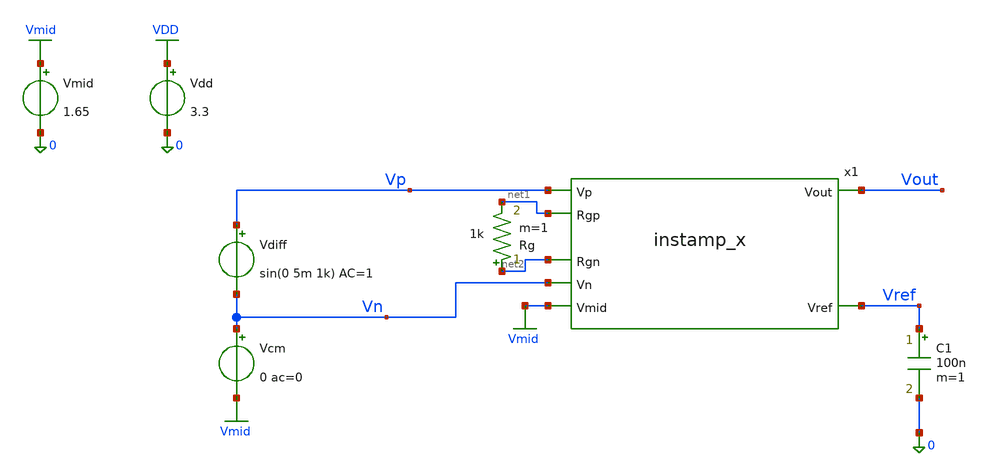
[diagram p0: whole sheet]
** sch_path: xschem/instamp_x_tb.sch
* Copyright 2021 Stefan Frederik Schippers
* Licensed under the Apache License, Version 2.0 (the "License");
* you may not use this file except in compliance with the License.
* You may obtain a copy of the License at
* https://www.apache.org/licenses/LICENSE-2.0
* Unless required by applicable law or agreed to in writing, software
* distributed under the License is distributed on an "AS IS" BASIS,
* WITHOUT WARRANTIES OR CONDITIONS OF ANY KIND, either express or implied.
* See the License for the specific language governing permissions and
* limitations under the License.
**.subckt instamp_x_tb
Vdd VDD 0 3.3
C1 Vref 0 100n m=1
Vdiff Vp Vn sin(0 5m 1k) AC=1
Vmid Vmid 0 1.65
x1 Vp Vmid net1 Vout Vref Vn net2 instamp_x
Rg net2 net1 1k m=1
Vcm Vn Vmid 0 ac=0
**** begin user architecture code

** opencircuitdesign pdks install
.lib $::SKYWATER_MODELS/sky130.lib.spice tt



.option wnflag=1
.option savecurrents
.save all
.control
op
write instamp_x_tb.raw
set appendwrite
set gnuplot_terminal=png/quit

* write instamp_x_tb.raw
if 0
* differential gain tran
  destroy all
  foreach val 90k 5k 1k
    alter Rg = $val
    tran 10u 3m 1m
  end
  let Rg90k = tran1.v(vout)
  let Rg5k = tran2.v(vout)
  let Rg1k = tran3.v(vout)
  gnuplot tran Rg90k Rg5k Rg1k
*+ title 'Differential gain'  xlabel 'Time' ylabel 'Volts'
endif

* run ac on schematic as drawn
if 0
  destroy all
* differential gain ac
  ac dec 100 1 1Meg
  plot db(v(vout))
endif

* run ac cmrr and psrr sweeps
if 1
  destroy all
* differential gain ac
  alter vdiff ac=1
  alter vcm ac=0
  alter vdd ac=0
  foreach val 90k 5k 1k
    alter Rg = $val
    ac dec 100 1 1Meg
  end
  alter vdiff ac=0
  alter vcm ac=1
  alter vdd ac=0
  foreach val 90k 5k 1k
    alter Rg = $val
    ac dec 100 1 1Meg
  end
  alter vdiff ac=0
  alter vcm ac=0
  alter vdd ac=1
  foreach val 90k 5k 1k
    alter Rg = $val
    ac dec 100 1 1Meg
  end
  alter vdiff ac=0
  alter vcm ac=0
  alter vdd ac=0
  alter vmid ac=1
  foreach val 90k 5k 1k
    alter Rg = $val
    ac dec 100 1 1Meg
  end
  let Rg90k = db(ac1.v(vout))
  let Rg5k = db(ac2.v(vout))
  let Rg1k = db(ac3.v(vout))
  let Rg90k_cm = Rg90k-db(ac4.v(vout))
  let Rg5k_cm = Rg5k-db(ac5.v(vout))
  let Rg1k_cm = Rg1k-db(ac6.v(vout))
  let Rg90k_psh = Rg90k-db(ac7.v(vout))
  let Rg5k_psh = Rg5k-db(ac8.v(vout))
  let Rg1k_psh = Rg1k-db(ac9.v(vout))
  let Rg90k_vmid = Rg90k-db(ac10.v(vout))
  let Rg5k_vmid = Rg5k-db(ac11.v(vout))
  let Rg1k_vmid = Rg1k-db(ac12.v(vout))

  gnuplot ac Rg90k Rg5k Rg1k  title 'Differential gain'  xlabel 'Freq' ylabel 'Gain dB'
  gnuplot cmrr Rg90k_cm Rg5k_cm Rg1k_cm  title 'CMRR'  xlabel 'Freq' ylabel 'Gain dB'
  gnuplot psrr Rg90k_psh Rg5k_psh Rg1k_psh  title 'PSRR'  xlabel 'Freq' ylabel 'Gain dB'
  gnuplot vmid_rej Rg90k_vmid Rg5k_vmid Rg1k_vmid  title 'Vmid Rejection'  xlabel 'Freq' ylabel 'Gain dB'

endif

if 0
* common mode gain
  alter vdiff ac=0
  alter vcm ac=1
  foreach val 90k 5k 1k
    alter Rg = $val
    ac dec 100 1 10Meg
  end

  plot db(ac1.V(Vout)) db(ac2.V(Vout))   db(ac3.V(Vout)) title 'Mag Vout'

* power supply gain
  alter vcm ac=0
  alter vdd ac=1
  foreach val 90k 5k 1k
    alter Rg = $val
    ac dec 100 1 10Meg
  end

  plot db(ac4.V(Vout)) db(ac5.V(Vout))   db(ac6.V(Vout)) title 'Mag Vout'

endif

.endc


**** end user architecture code
**.ends
.GLOBAL VDD
.GLOBAL Vmid
.end
